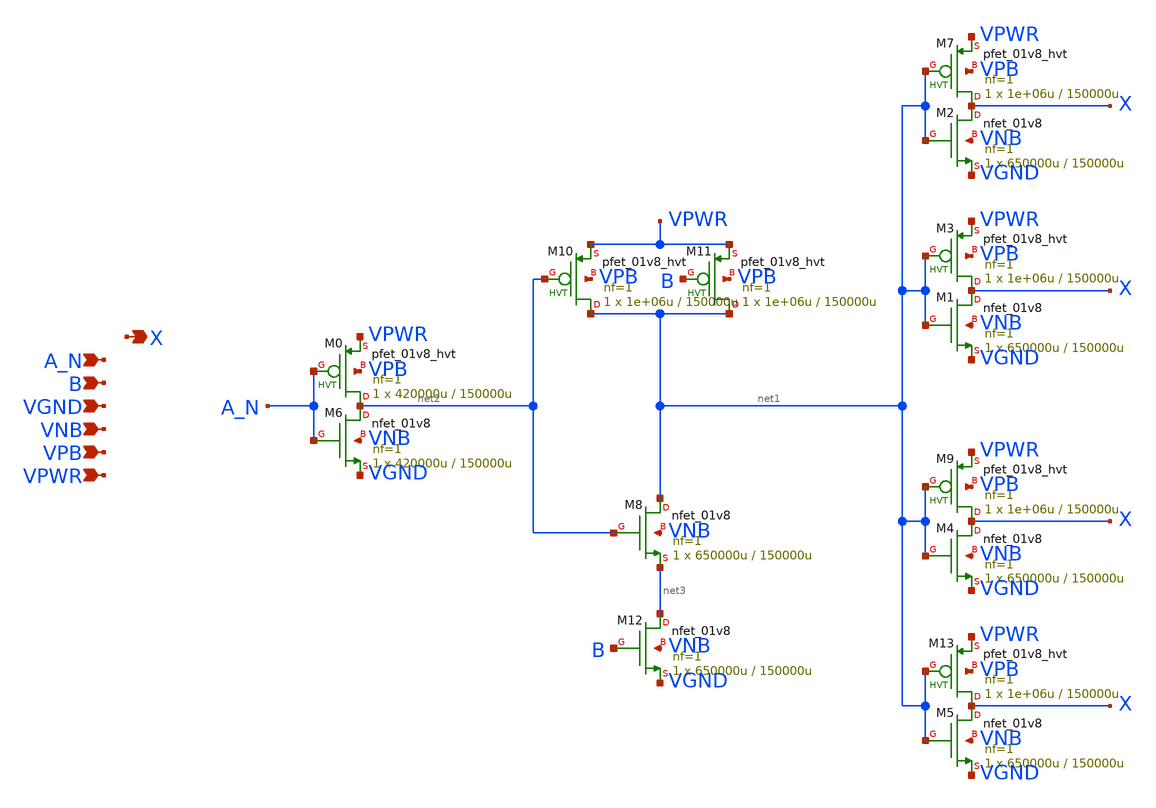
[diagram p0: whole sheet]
** sch_path: schematics/and2b/sky130_fd_sc_hd__and2b_4.sch
**.subckt sky130_fd_sc_hd__and2b_4 A_N B VGND VNB VPB VPWR X
*.ipin A_N
*.ipin B
*.ipin VGND
*.ipin VNB
*.ipin VPB
*.ipin VPWR
*.opin X
XM3 X net1 VPWR VPB sky130_fd_pr__pfet_01v8_hvt L=150000u W=1e+06u nf=1 ad='int((1 + 1)/2) * 1e+06u / 1 * 0.29'
+ as='int((1 + 2)/2) * 1e+06u / 1 * 0.29' pd='2*int((1 + 1)/2) * (1e+06u / 1 + 0.29)' ps='2*int((1 + 2)/2) * (1e+06u / 1 + 0.29)'
+ nrd='0.29 / 1e+06u ' nrs='0.29 / 1e+06u ' sa=0 sb=0 sd=0 mult=1 m=1
XM1 X net1 VGND VNB sky130_fd_pr__nfet_01v8 L=150000u W=650000u nf=1 ad='int((1 + 1)/2) * 650000u / 1 * 0.29'
+ as='int((1 + 2)/2) * 650000u / 1 * 0.29' pd='2*int((1 + 1)/2) * (650000u / 1 + 0.29)' ps='2*int((1 + 2)/2) * (650000u / 1 + 0.29)'
+ nrd='0.29 / 650000u ' nrs='0.29 / 650000u ' sa=0 sb=0 sd=0 mult=1 m=1
XM7 X net1 VPWR VPB sky130_fd_pr__pfet_01v8_hvt L=150000u W=1e+06u nf=1 ad='int((1 + 1)/2) * 1e+06u / 1 * 0.29'
+ as='int((1 + 2)/2) * 1e+06u / 1 * 0.29' pd='2*int((1 + 1)/2) * (1e+06u / 1 + 0.29)' ps='2*int((1 + 2)/2) * (1e+06u / 1 + 0.29)'
+ nrd='0.29 / 1e+06u ' nrs='0.29 / 1e+06u ' sa=0 sb=0 sd=0 mult=1 m=1
XM2 X net1 VGND VNB sky130_fd_pr__nfet_01v8 L=150000u W=650000u nf=1 ad='int((1 + 1)/2) * 650000u / 1 * 0.29'
+ as='int((1 + 2)/2) * 650000u / 1 * 0.29' pd='2*int((1 + 1)/2) * (650000u / 1 + 0.29)' ps='2*int((1 + 2)/2) * (650000u / 1 + 0.29)'
+ nrd='0.29 / 650000u ' nrs='0.29 / 650000u ' sa=0 sb=0 sd=0 mult=1 m=1
XM9 X net1 VPWR VPB sky130_fd_pr__pfet_01v8_hvt L=150000u W=1e+06u nf=1 ad='int((1 + 1)/2) * 1e+06u / 1 * 0.29'
+ as='int((1 + 2)/2) * 1e+06u / 1 * 0.29' pd='2*int((1 + 1)/2) * (1e+06u / 1 + 0.29)' ps='2*int((1 + 2)/2) * (1e+06u / 1 + 0.29)'
+ nrd='0.29 / 1e+06u ' nrs='0.29 / 1e+06u ' sa=0 sb=0 sd=0 mult=1 m=1
XM4 X net1 VGND VNB sky130_fd_pr__nfet_01v8 L=150000u W=650000u nf=1 ad='int((1 + 1)/2) * 650000u / 1 * 0.29'
+ as='int((1 + 2)/2) * 650000u / 1 * 0.29' pd='2*int((1 + 1)/2) * (650000u / 1 + 0.29)' ps='2*int((1 + 2)/2) * (650000u / 1 + 0.29)'
+ nrd='0.29 / 650000u ' nrs='0.29 / 650000u ' sa=0 sb=0 sd=0 mult=1 m=1
XM13 X net1 VPWR VPB sky130_fd_pr__pfet_01v8_hvt L=150000u W=1e+06u nf=1 ad='int((1 + 1)/2) * 1e+06u / 1 * 0.29'
+ as='int((1 + 2)/2) * 1e+06u / 1 * 0.29' pd='2*int((1 + 1)/2) * (1e+06u / 1 + 0.29)' ps='2*int((1 + 2)/2) * (1e+06u / 1 + 0.29)'
+ nrd='0.29 / 1e+06u ' nrs='0.29 / 1e+06u ' sa=0 sb=0 sd=0 mult=1 m=1
XM5 X net1 VGND VNB sky130_fd_pr__nfet_01v8 L=150000u W=650000u nf=1 ad='int((1 + 1)/2) * 650000u / 1 * 0.29'
+ as='int((1 + 2)/2) * 650000u / 1 * 0.29' pd='2*int((1 + 1)/2) * (650000u / 1 + 0.29)' ps='2*int((1 + 2)/2) * (650000u / 1 + 0.29)'
+ nrd='0.29 / 650000u ' nrs='0.29 / 650000u ' sa=0 sb=0 sd=0 mult=1 m=1
XM0 net2 A_N VPWR VPB sky130_fd_pr__pfet_01v8_hvt L=150000u W=420000u nf=1 ad='int((1 + 1)/2) * 420000u / 1 * 0.29'
+ as='int((1 + 2)/2) * 420000u / 1 * 0.29' pd='2*int((1 + 1)/2) * (420000u / 1 + 0.29)' ps='2*int((1 + 2)/2) * (420000u / 1 + 0.29)'
+ nrd='0.29 / 420000u ' nrs='0.29 / 420000u ' sa=0 sb=0 sd=0 mult=1 m=1
XM6 net2 A_N VGND VNB sky130_fd_pr__nfet_01v8 L=150000u W=420000u nf=1 ad='int((1 + 1)/2) * 420000u / 1 * 0.29'
+ as='int((1 + 2)/2) * 420000u / 1 * 0.29' pd='2*int((1 + 1)/2) * (420000u / 1 + 0.29)' ps='2*int((1 + 2)/2) * (420000u / 1 + 0.29)'
+ nrd='0.29 / 420000u ' nrs='0.29 / 420000u ' sa=0 sb=0 sd=0 mult=1 m=1
XM10 net1 net2 VPWR VPB sky130_fd_pr__pfet_01v8_hvt L=150000u W=1e+06u nf=1 ad='int((1 + 1)/2) * 1e+06u / 1 * 0.29'
+ as='int((1 + 2)/2) * 1e+06u / 1 * 0.29' pd='2*int((1 + 1)/2) * (1e+06u / 1 + 0.29)' ps='2*int((1 + 2)/2) * (1e+06u / 1 + 0.29)'
+ nrd='0.29 / 1e+06u ' nrs='0.29 / 1e+06u ' sa=0 sb=0 sd=0 mult=1 m=1
XM11 net1 B VPWR VPB sky130_fd_pr__pfet_01v8_hvt L=150000u W=1e+06u nf=1 ad='int((1 + 1)/2) * 1e+06u / 1 * 0.29'
+ as='int((1 + 2)/2) * 1e+06u / 1 * 0.29' pd='2*int((1 + 1)/2) * (1e+06u / 1 + 0.29)' ps='2*int((1 + 2)/2) * (1e+06u / 1 + 0.29)'
+ nrd='0.29 / 1e+06u ' nrs='0.29 / 1e+06u ' sa=0 sb=0 sd=0 mult=1 m=1
XM8 net1 net2 net3 VNB sky130_fd_pr__nfet_01v8 L=150000u W=650000u nf=1 ad='int((1 + 1)/2) * 650000u / 1 * 0.29'
+ as='int((1 + 2)/2) * 650000u / 1 * 0.29' pd='2*int((1 + 1)/2) * (650000u / 1 + 0.29)' ps='2*int((1 + 2)/2) * (650000u / 1 + 0.29)'
+ nrd='0.29 / 650000u ' nrs='0.29 / 650000u ' sa=0 sb=0 sd=0 mult=1 m=1
XM12 net3 B VGND VNB sky130_fd_pr__nfet_01v8 L=150000u W=650000u nf=1 ad='int((1 + 1)/2) * 650000u / 1 * 0.29'
+ as='int((1 + 2)/2) * 650000u / 1 * 0.29' pd='2*int((1 + 1)/2) * (650000u / 1 + 0.29)' ps='2*int((1 + 2)/2) * (650000u / 1 + 0.29)'
+ nrd='0.29 / 650000u ' nrs='0.29 / 650000u ' sa=0 sb=0 sd=0 mult=1 m=1
**.ends
.end
